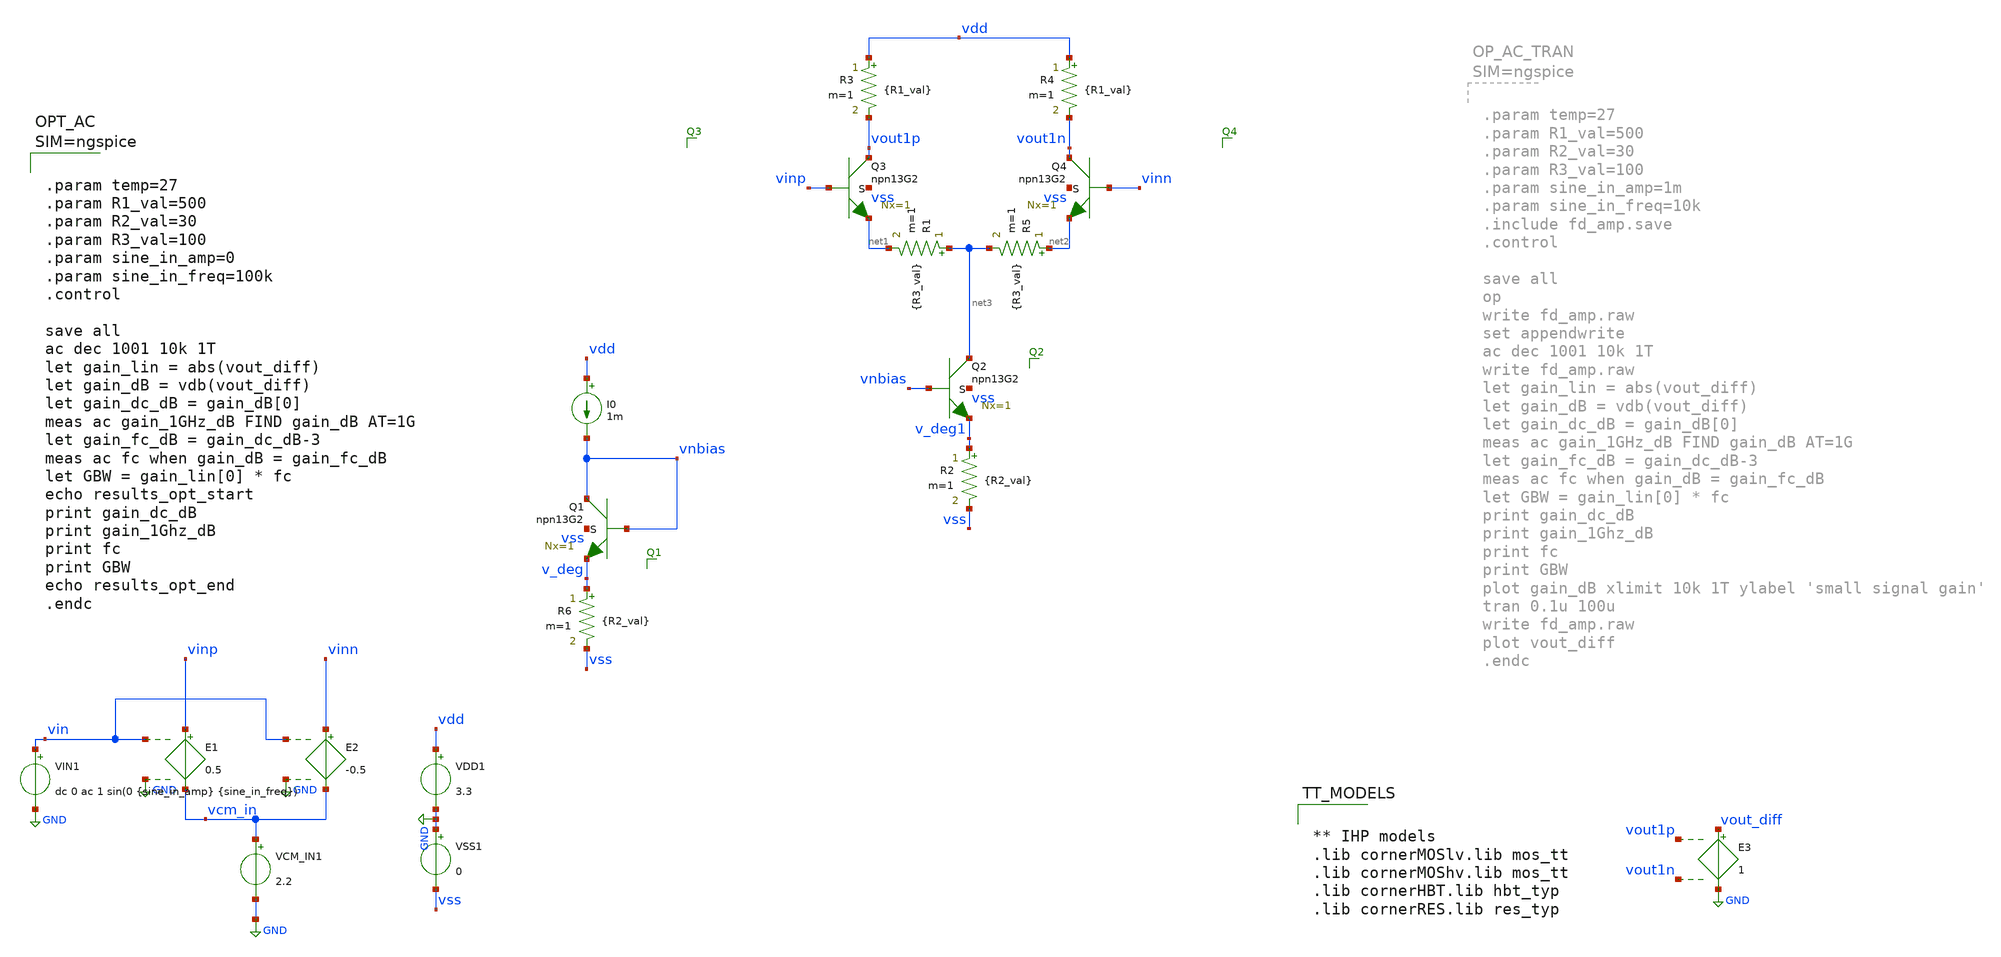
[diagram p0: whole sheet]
** sch_path: ngspice/fd_amp.sch
**.subckt fd_amp
VDD1 vdd GND 3.3
VSS1 GND vss 0
E1 vinp vcm_in vin GND 0.5
E2 vinn vcm_in vin GND -0.5
VCM_IN1 vcm_in GND 2.2
VIN1 vin GND dc 0 ac 1 sin(0 {sine_in_amp} {sine_in_freq})
E3 vout_diff GND vout1p vout1n 1
XQ3 vout1p vinp net1 vss npn13G2 Nx=1 mm_ok=1
XQ4 vout1n vinn net2 vss npn13G2 Nx=1 mm_ok=1
R2 v_deg1 vss {R2_val} m=1
XQ2 net3 vnbias v_deg1 vss npn13G2 Nx=1 mm_ok=1
R3 vdd vout1p {R1_val} m=1
R4 vdd vout1n {R1_val} m=1
R1 net3 net1 {R3_val} m=1
R5 net2 net3 {R3_val} m=1
XQ1 vnbias vnbias v_deg vss npn13G2 Nx=1 mm_ok=1
I0 vdd vnbias 1m
R6 v_deg vss {R2_val} m=1
**** begin user architecture code


** IHP models
.lib cornerMOSlv.lib mos_tt
.lib cornerMOShv.lib mos_tt
.lib cornerHBT.lib hbt_typ
.lib cornerRES.lib res_typ





.param temp=27
.param R1_val=500
.param R2_val=30
.param R3_val=100
.param sine_in_amp=0
.param sine_in_freq=100k
.control

save all
ac dec 1001 10k 1T
let gain_lin = abs(vout_diff)
let gain_dB = vdb(vout_diff)
let gain_dc_dB = gain_dB[0]
meas ac gain_1GHz_dB FIND gain_dB AT=1G
let gain_fc_dB = gain_dc_dB-3
meas ac fc when gain_dB = gain_fc_dB
let GBW = gain_lin[0] * fc
echo results_opt_start
print gain_dc_dB
print gain_1Ghz_dB
print fc
print GBW
echo results_opt_end
.endc



**** end user architecture code
**.ends
.GLOBAL GND
.end
